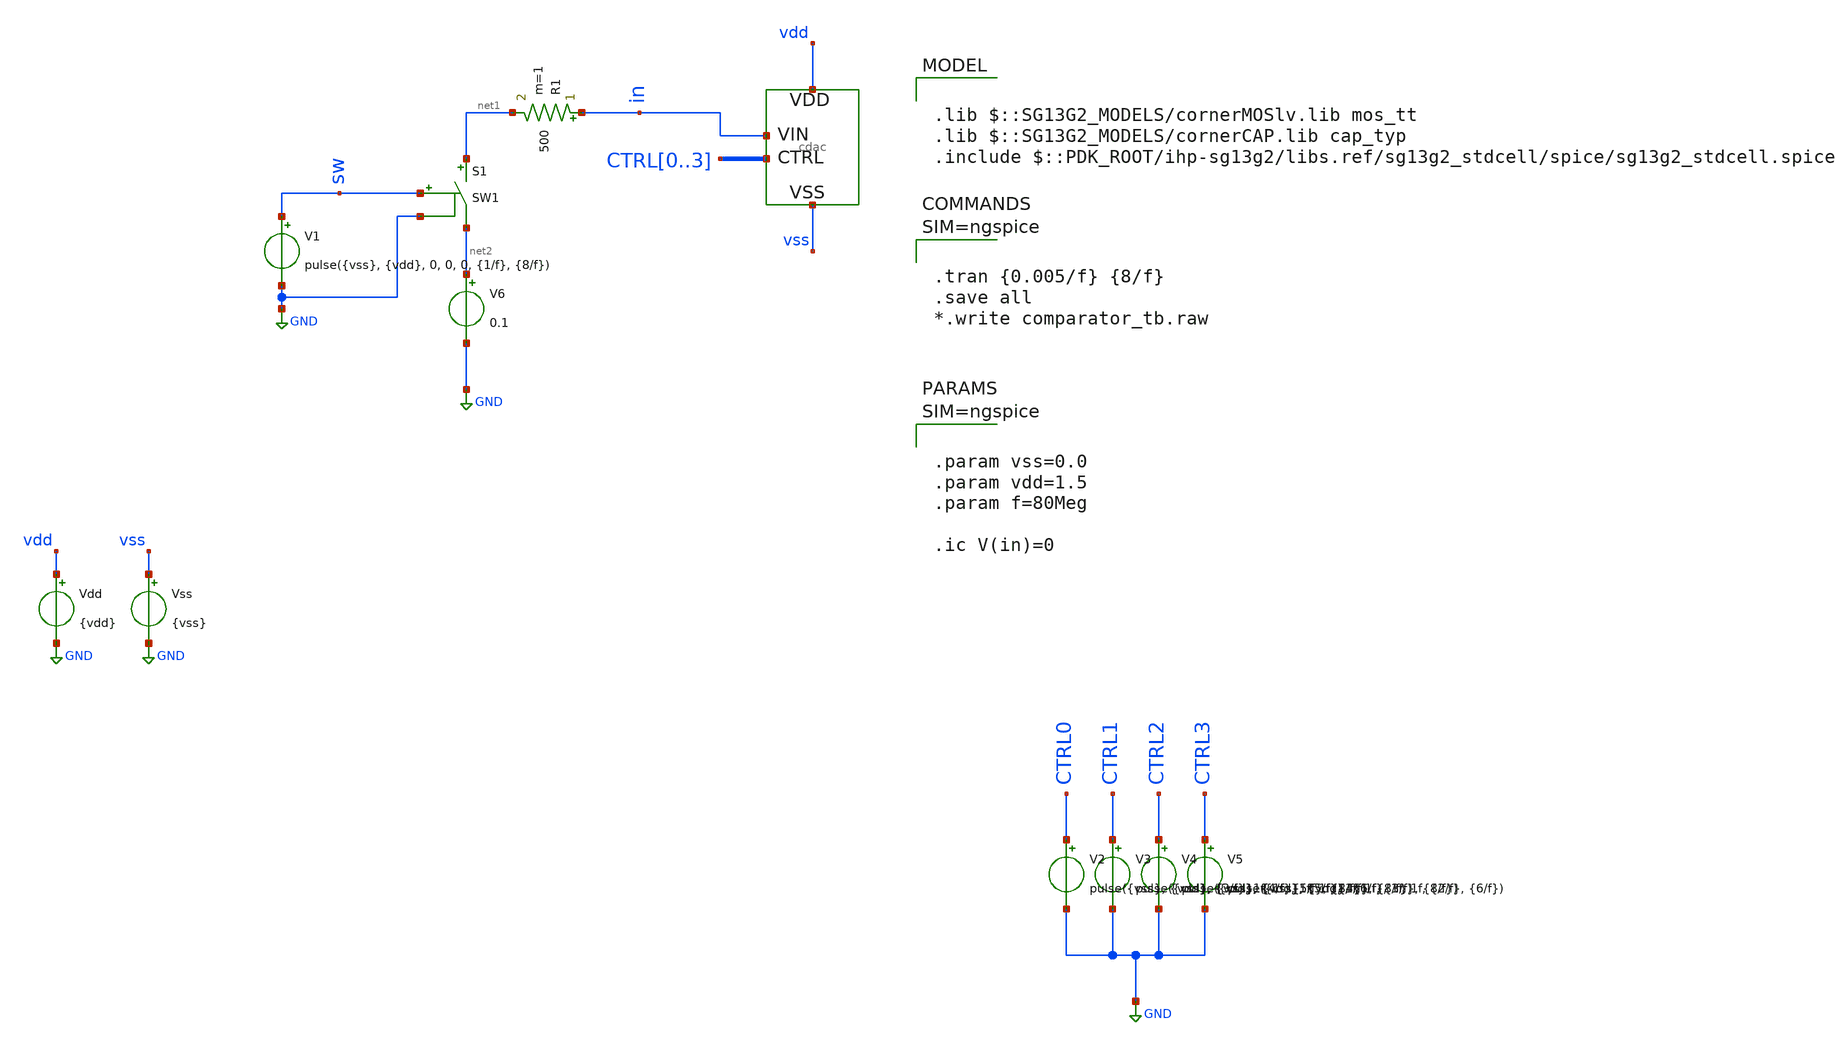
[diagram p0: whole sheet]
** sch_path: designs/cdac/cdac_tb.sch
* IHP-GmbH/IHP-Open-PDK/ihp-sg13g2/libs.tech/xschem/sg13g2_stdcells/sg13g2_inv_2.sch:
* Copyright 2023 IHP PDK Authors
* Licensed under the Apache License, Version 2.0 (the "License");
**.subckt cdac_tb
x1 in CTRL0 CTRL1 CTRL2 CTRL3 vss vdd cdac
S1 net1 net2 sw GND SW1
R1 in net1 500 m=1
V1 sw GND pulse({vss}, {vdd}, 0, 0, 0, {1/f}, {8/f})
Vdd vdd GND {vdd}
Vss vss GND {vss}
V2 CTRL0 GND pulse({vss}, {vdd}, {3/f}, 1f, 1f, {5/f}, {8/f})
V3 CTRL1 GND pulse({vss}, {vdd}, {4/f}, 1f, 1f, {4/f}, {8/f})
V4 CTRL2 GND pulse({vss}, {vdd}, {5/f}, 1f, 1f, {3/f}, {8/f})
V5 CTRL3 GND pulse({vss}, {vdd}, {6/f}, 1f, 1f, {2/f}, {6/f})
V6 net2 GND 0.1
**** begin user architecture code

.lib $::SG13G2_MODELS/cornerMOSlv.lib mos_tt
.lib $::SG13G2_MODELS/cornerCAP.lib cap_typ
.include $::PDK_ROOT/ihp-sg13g2/libs.ref/sg13g2_stdcell/spice/sg13g2_stdcell.spice




.tran {0.005/f} {8/f}
.save all
*.write comparator_tb.raw






.param vss=0.0
.param vdd=1.5
.param f=80Meg

.ic V(in)=0



**** end user architecture code
**.ends

* expanding   symbol:  cdac.sym # of pins=4
** sym_path: designs/cdac/cdac.sym
** sch_path: designs/cdac/cdac.sch
.subckt cdac VIN CTRL0 CTRL1 CTRL2 CTRL3 VSS VDD
*.ipin VIN
*.ipin CTRL0,CTRL1,CTRL2,CTRL3
*.ipin VSS
*.ipin VDD
XC1 VIN l1 cap_cmim w=2.577e-5 l=2.577e-5 m=1 mm_ok=1
XC2 VIN l2 cap_cmim w=1.820e-5 l=1.820e-5 m=1 mm_ok=1
XC3 VIN l3 cap_cmim w=1.286e-5 l=1.286e-5 m=1 mm_ok=1
XC4 VIN l4 cap_cmim w=9.076e-6 l=9.076e-6 m=1 mm_ok=1
XC5 VIN VSS cap_cmim w=9.076e-6 l=9.076e-6 m=1 mm_ok=1
x1 l1 CTRL0 VDD VSS sg13g2_inv_2
x2 l2 CTRL1 VDD VSS sg13g2_inv_2
x3 l3 CTRL2 VDD VSS sg13g2_inv_2
x4 l4 CTRL3 VDD VSS sg13g2_inv_2
.ends


* expanding   symbol:  sg13g2_stdcells/sg13g2_inv_2.sym # of pins=2
** sym_path: sg13g2_stdcells/sg13g2_inv_2.sym
** sch_path: sg13g2_stdcells/sg13g2_inv_2.sch
.subckt sg13g2_inv_2 Y A VDD VSS
*.opin Y
*.ipin A
*.iopin VDD
*.iopin VSS
XM1 Y A VSS VSS sg13_lv_nmos w=1.48u l=130.00n ng=2 m=1 mm_ok=1
XM2 Y A VDD VDD sg13_lv_pmos w=2.24u l=130.00n ng=2 m=1 mm_ok=1
.ends

.GLOBAL GND
**** begin user architecture code
.MODEL SW1 SW   VT=0.9 VH=0.01  RON=0.01 ROFF=10G
**** end user architecture code
.end
